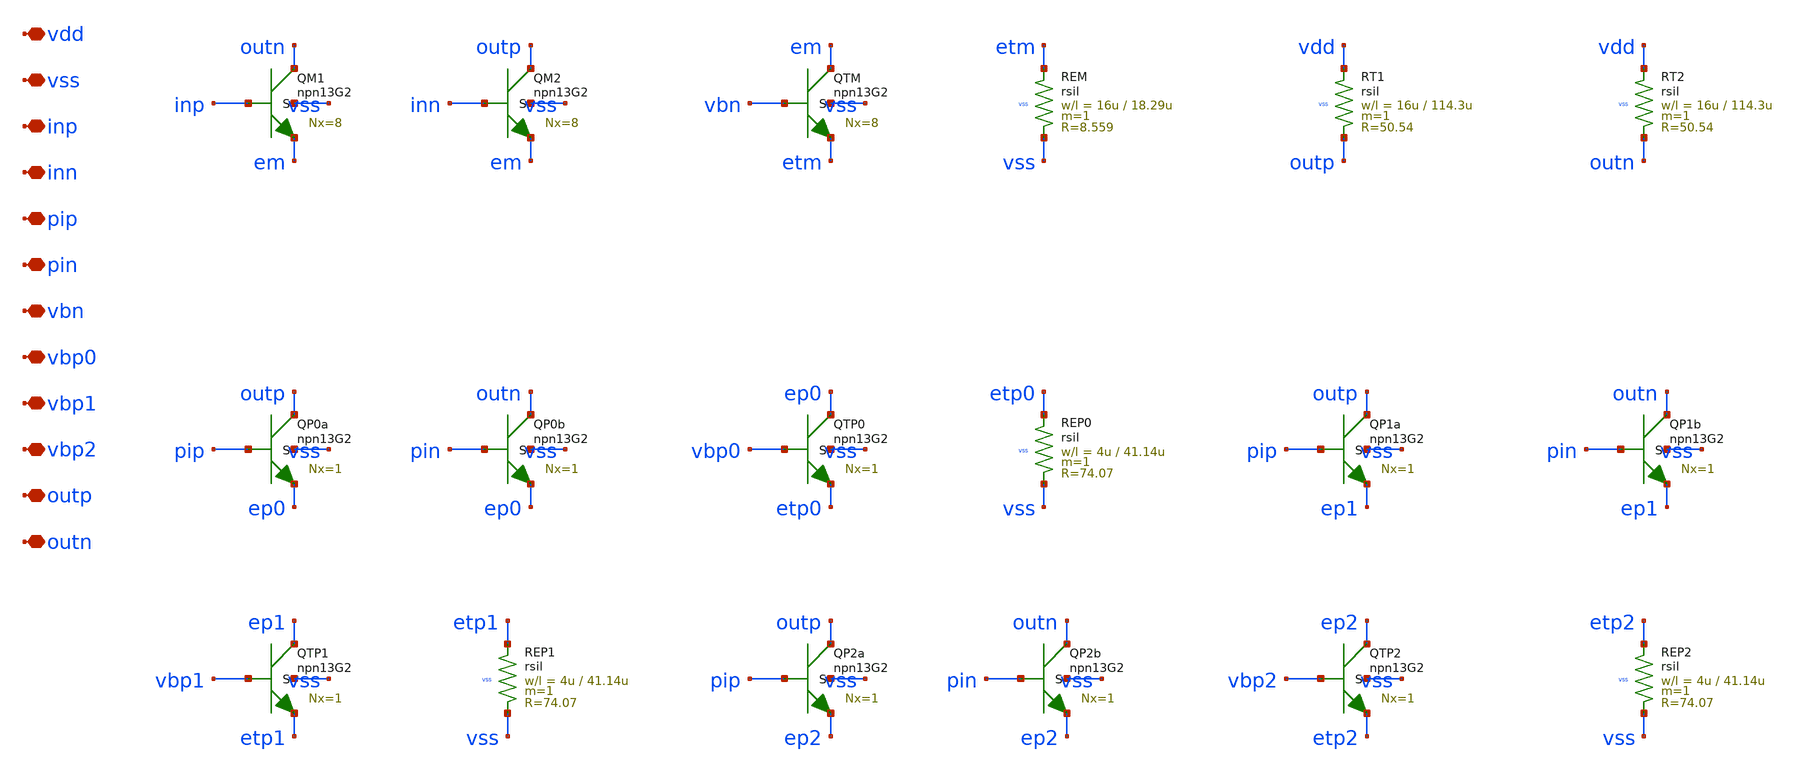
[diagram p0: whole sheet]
** sch_path: design/tx/driver_ffe.sch
**.subckt driver_ffe vdd vss inp inn pip pin vbn vbp0 vbp1 vbp2 outp outn
*.iopin vdd
*.iopin vss
*.iopin inp
*.iopin inn
*.iopin pip
*.iopin pin
*.iopin vbn
*.iopin vbp0
*.iopin vbp1
*.iopin vbp2
*.iopin outp
*.iopin outn
XQM1 outn inp em vss npn13G2 Nx=8 mm_ok=1
XQM2 outp inn em vss npn13G2 Nx=8 mm_ok=1
XQTM em vbn etm vss npn13G2 Nx=8 mm_ok=1
XREM etm vss vss rsil w=16u l=18.29u m=1 mm_ok=1
XRT1 vdd outp vss rsil w=16u l=114.3u m=1 mm_ok=1
XRT2 vdd outn vss rsil w=16u l=114.3u m=1 mm_ok=1
XQP0a outp pip ep0 vss npn13G2 Nx=1 mm_ok=1
XQP0b outn pin ep0 vss npn13G2 Nx=1 mm_ok=1
XQTP0 ep0 vbp0 etp0 vss npn13G2 Nx=1 mm_ok=1
XREP0 etp0 vss vss rsil w=4u l=41.14u m=1 mm_ok=1
XQP1a outp pip ep1 vss npn13G2 Nx=1 mm_ok=1
XQP1b outn pin ep1 vss npn13G2 Nx=1 mm_ok=1
XQTP1 ep1 vbp1 etp1 vss npn13G2 Nx=1 mm_ok=1
XREP1 etp1 vss vss rsil w=4u l=41.14u m=1 mm_ok=1
XQP2a outp pip ep2 vss npn13G2 Nx=1 mm_ok=1
XQP2b outn pin ep2 vss npn13G2 Nx=1 mm_ok=1
XQTP2 ep2 vbp2 etp2 vss npn13G2 Nx=1 mm_ok=1
XREP2 etp2 vss vss rsil w=4u l=41.14u m=1 mm_ok=1
**.ends
.end
